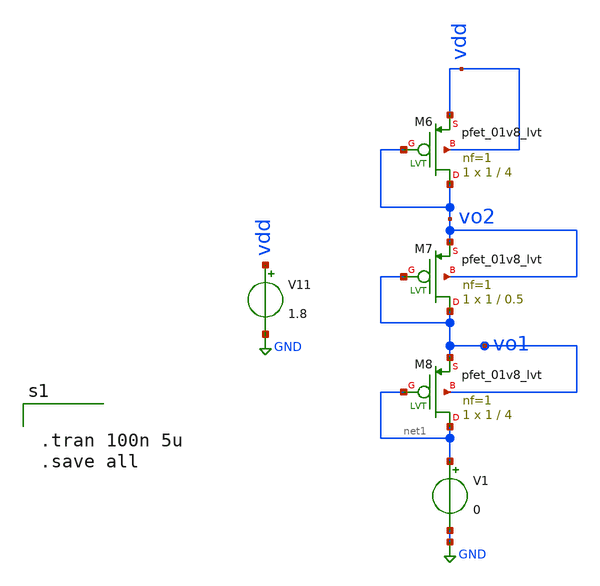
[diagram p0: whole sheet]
** sch_path: xschem/xschemfiles/ref_generator.sch
**.subckt ref_generator
V11 vdd GND 1.8
V1 net1 GND 0
XM6 vo2 vo2 vdd vdd sky130_fd_pr__pfet_01v8_lvt L=4 W=1 nf=1 ad='int((nf+1)/2) * W/nf * 0.29' as='int((nf+2)/2) * W/nf * 0.29'
+ pd='2*int((nf+1)/2) * (W/nf + 0.29)' ps='2*int((nf+2)/2) * (W/nf + 0.29)' nrd='0.29 / W' nrs='0.29 / W'
+ sa=0 sb=0 sd=0 mult=1 m=1
XM7 vo1 vo1 vo2 vo2 sky130_fd_pr__pfet_01v8_lvt L=0.5 W=1 nf=1 ad='int((nf+1)/2) * W/nf * 0.29' as='int((nf+2)/2) * W/nf * 0.29'
+ pd='2*int((nf+1)/2) * (W/nf + 0.29)' ps='2*int((nf+2)/2) * (W/nf + 0.29)' nrd='0.29 / W' nrs='0.29 / W'
+ sa=0 sb=0 sd=0 mult=1 m=1
XM8 net1 net1 vo1 vo1 sky130_fd_pr__pfet_01v8_lvt L=4 W=1 nf=1 ad='int((nf+1)/2) * W/nf * 0.29' as='int((nf+2)/2) * W/nf * 0.29'
+ pd='2*int((nf+1)/2) * (W/nf + 0.29)' ps='2*int((nf+2)/2) * (W/nf + 0.29)' nrd='0.29 / W' nrs='0.29 / W'
+ sa=0 sb=0 sd=0 mult=1 m=1
**** begin user architecture code

** opencircuitdesign pdks install
.lib $::SKYWATER_MODELS/sky130.lib.spice tt




.tran 100n 5u
.save all


**** end user architecture code
**.ends
.GLOBAL GND
.end
